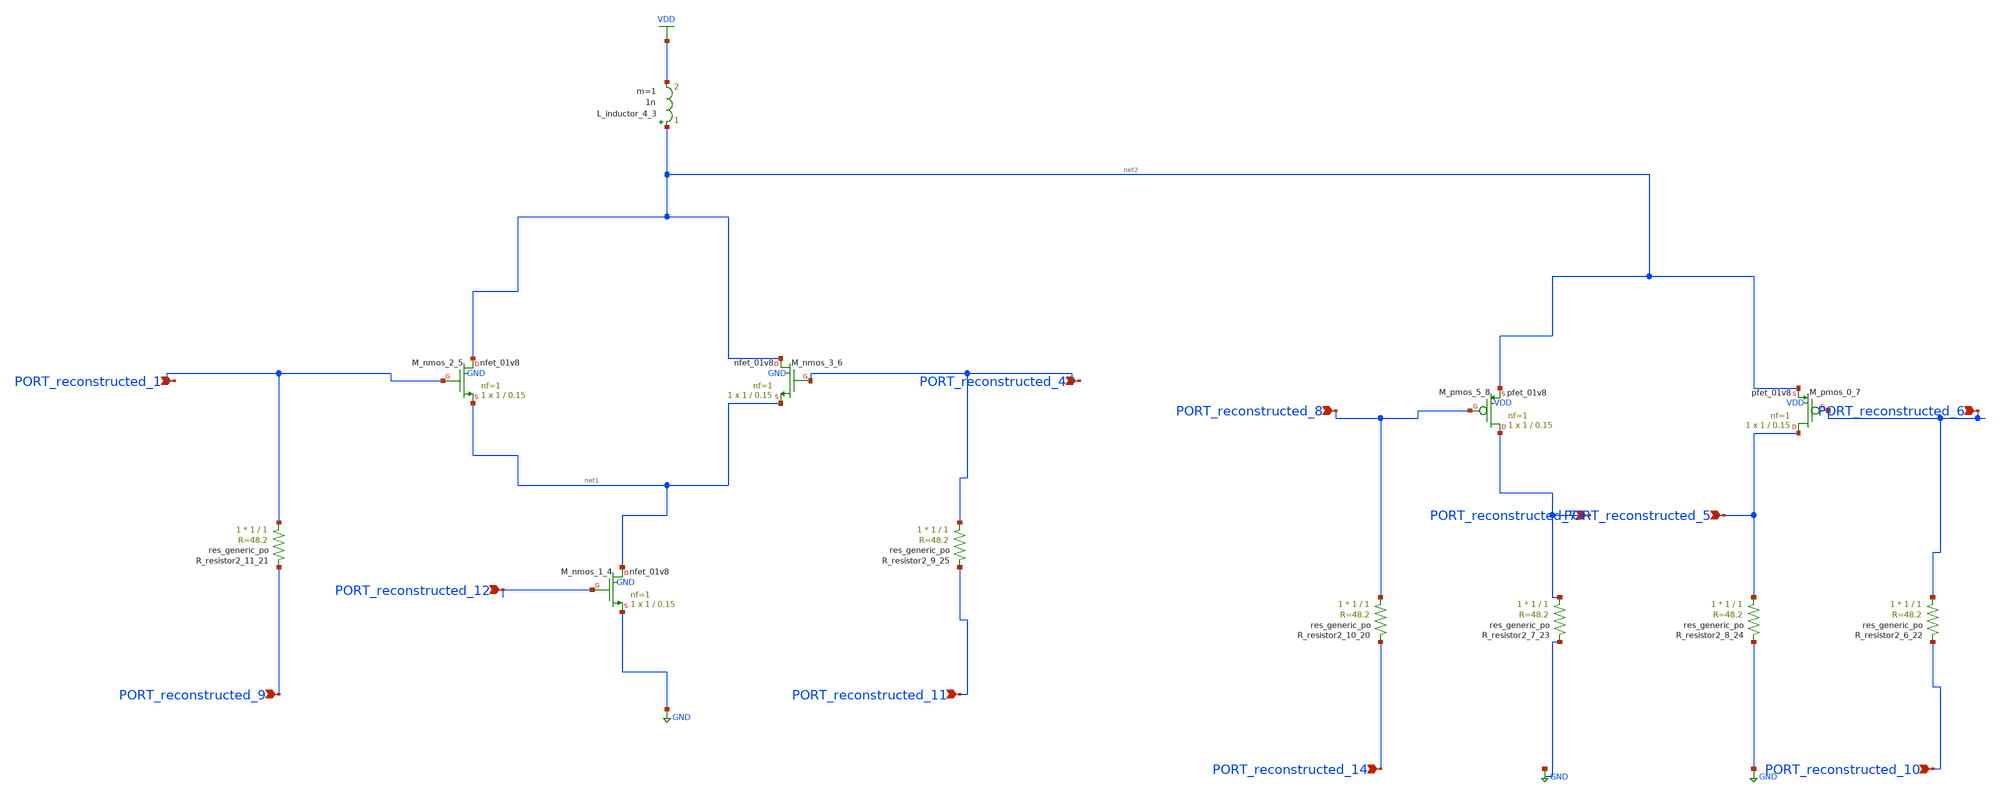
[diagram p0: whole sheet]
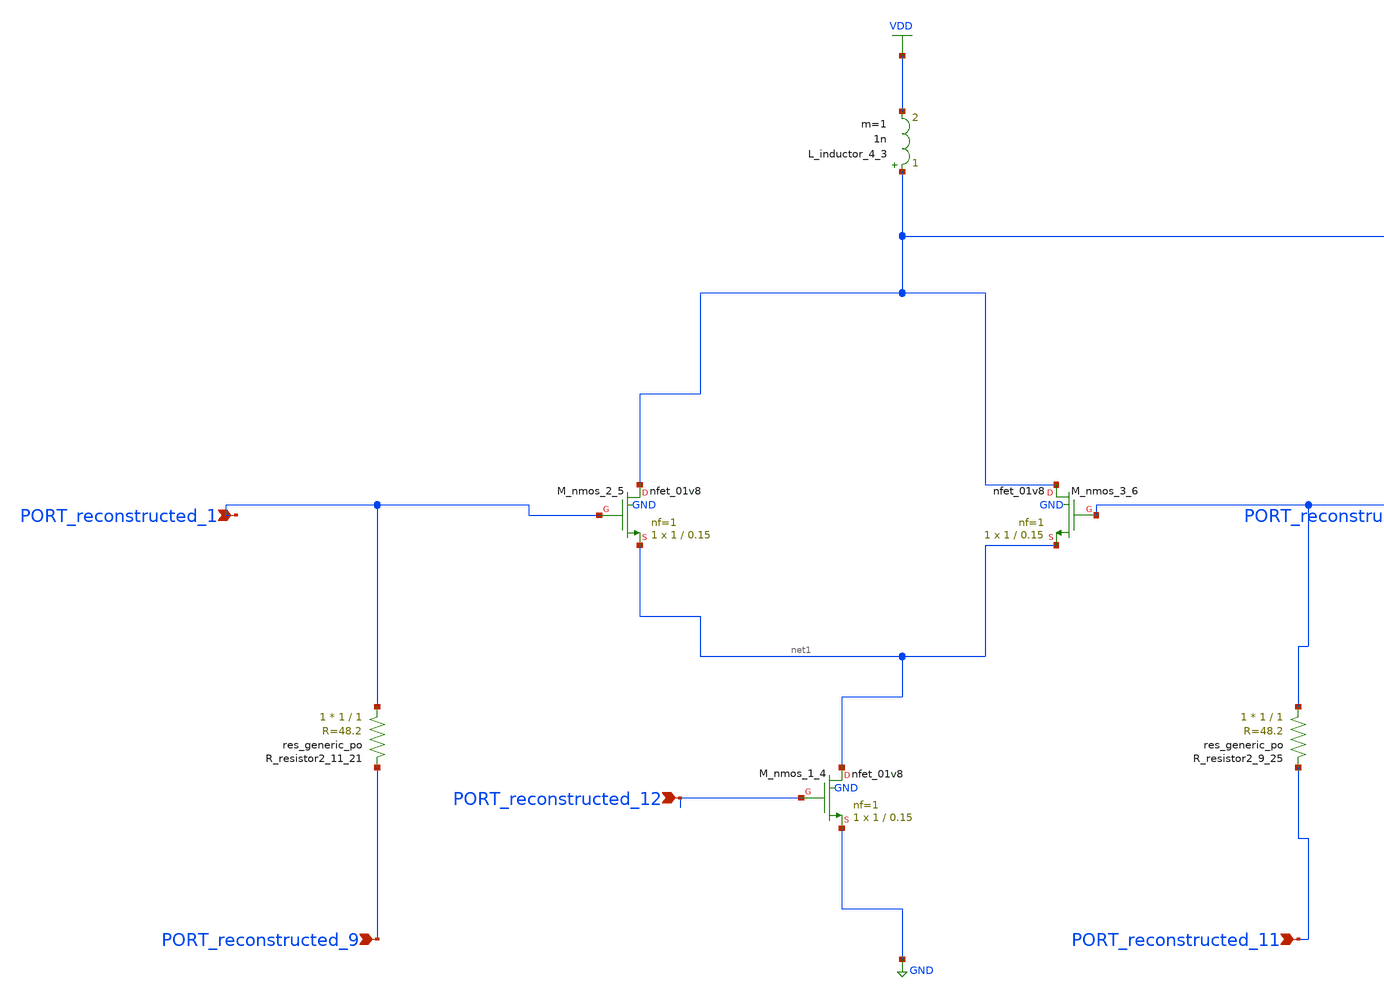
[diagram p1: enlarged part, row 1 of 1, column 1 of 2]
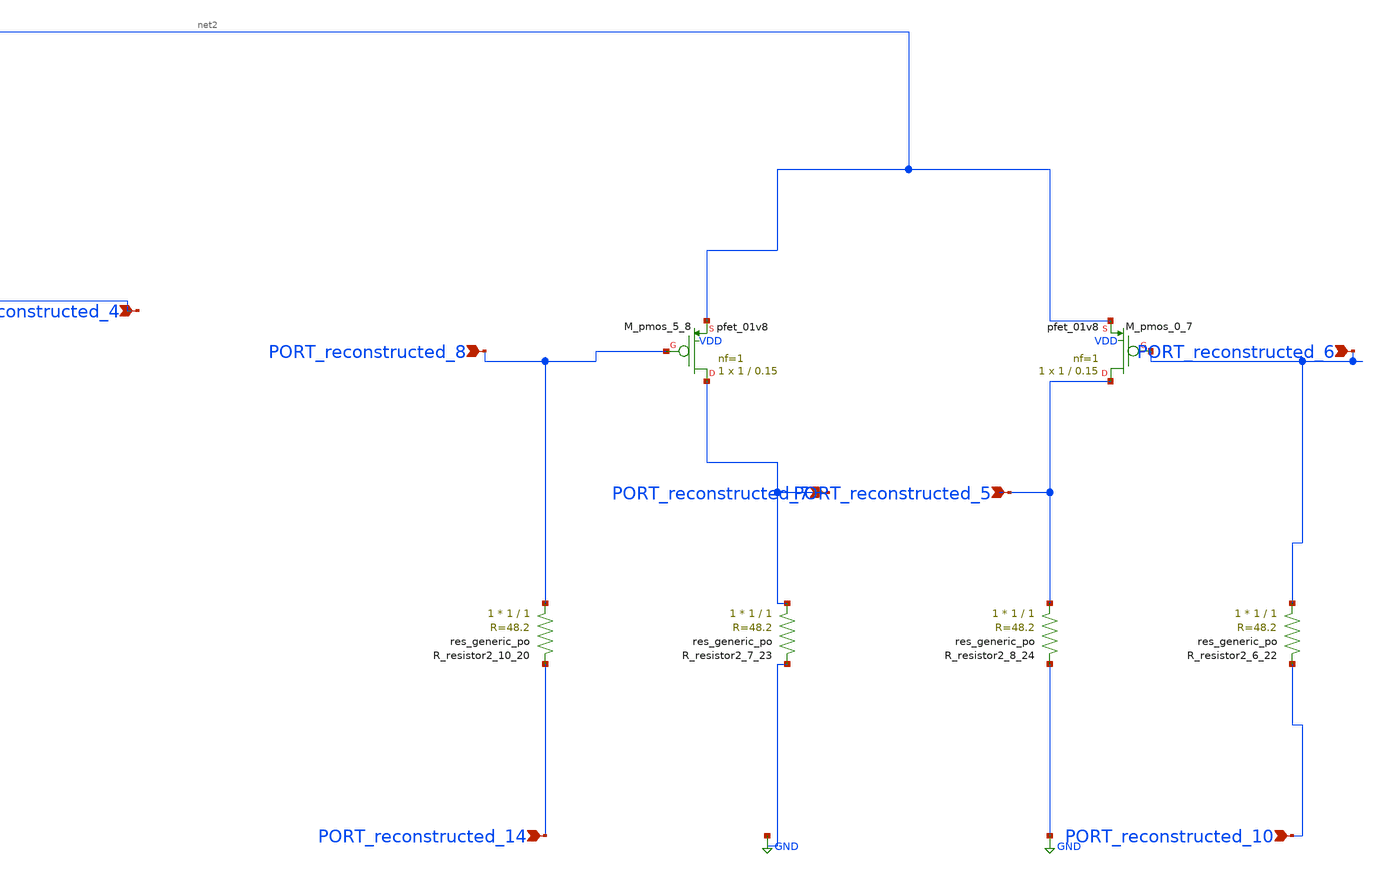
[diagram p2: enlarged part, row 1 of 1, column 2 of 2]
** sch_path: schematics/10_1016_j_aeue_2023_154684_09_004.sch
**.subckt 10_1016_j_aeue_2023_154684_09_004 PORT_reconstructed_1 PORT_reconstructed_6
*+ PORT_reconstructed_9 PORT_reconstructed_5 PORT_reconstructed_4 PORT_reconstructed_10 PORT_reconstructed_8
*+ PORT_reconstructed_7 PORT_reconstructed_11 PORT_reconstructed_12 PORT_reconstructed_14
*.ipin PORT_reconstructed_1
*.ipin PORT_reconstructed_6
*.ipin PORT_reconstructed_9
*.ipin PORT_reconstructed_5
*.ipin PORT_reconstructed_4
*.ipin PORT_reconstructed_10
*.ipin PORT_reconstructed_8
*.ipin PORT_reconstructed_7
*.ipin PORT_reconstructed_11
*.ipin PORT_reconstructed_12
*.ipin PORT_reconstructed_14
L_inductor_4_3 net2 VDD 1n m=1
XM_nmos_1_4 net1 PORT_reconstructed_12 GND GND sky130_fd_pr__nfet_01v8 L=0.15 W=1 nf=1 ad='int((1 + 1)/2) * 1 / 1 * 0.29'
+ as='int((1 + 2)/2) * 1 / 1 * 0.29' pd='2*int((1 + 1)/2) * (1 / 1 + 0.29)' ps='2*int((1 + 2)/2) * (1 / 1 + 0.29)'
+ nrd='0.29 / 1 ' nrs='0.29 / 1 ' sa=0 sb=0 sd=0 mult=1 m=1
XM_nmos_2_5 net2 PORT_reconstructed_1 net1 GND sky130_fd_pr__nfet_01v8 L=0.15 W=1 nf=1 ad='int((1 + 1)/2) * 1 / 1 * 0.29'
+ as='int((1 + 2)/2) * 1 / 1 * 0.29' pd='2*int((1 + 1)/2) * (1 / 1 + 0.29)' ps='2*int((1 + 2)/2) * (1 / 1 + 0.29)'
+ nrd='0.29 / 1 ' nrs='0.29 / 1 ' sa=0 sb=0 sd=0 mult=1 m=1
XM_nmos_3_6 net2 PORT_reconstructed_4 net1 GND sky130_fd_pr__nfet_01v8 L=0.15 W=1 nf=1 ad='int((1 + 1)/2) * 1 / 1 * 0.29'
+ as='int((1 + 2)/2) * 1 / 1 * 0.29' pd='2*int((1 + 1)/2) * (1 / 1 + 0.29)' ps='2*int((1 + 2)/2) * (1 / 1 + 0.29)'
+ nrd='0.29 / 1 ' nrs='0.29 / 1 ' sa=0 sb=0 sd=0 mult=1 m=1
XM_pmos_0_7 PORT_reconstructed_5 PORT_reconstructed_6 net2 VDD sky130_fd_pr__pfet_01v8 L=0.15 W=1 nf=1
+ ad='int((1 + 1)/2) * 1 / 1 * 0.29' as='int((1 + 2)/2) * 1 / 1 * 0.29' pd='2*int((1 + 1)/2) * (1 / 1 + 0.29)'
+ ps='2*int((1 + 2)/2) * (1 / 1 + 0.29)' nrd='0.29 / 1 ' nrs='0.29 / 1 ' sa=0 sb=0 sd=0 mult=1 m=1
XM_pmos_5_8 PORT_reconstructed_7 PORT_reconstructed_8 net2 VDD sky130_fd_pr__pfet_01v8 L=0.15 W=1 nf=1
+ ad='int((1 + 1)/2) * 1 / 1 * 0.29' as='int((1 + 2)/2) * 1 / 1 * 0.29' pd='2*int((1 + 1)/2) * (1 / 1 + 0.29)'
+ ps='2*int((1 + 2)/2) * (1 / 1 + 0.29)' nrd='0.29 / 1 ' nrs='0.29 / 1 ' sa=0 sb=0 sd=0 mult=1 m=1
XR_resistor2_10_20 PORT_reconstructed_8 PORT_reconstructed_14 sky130_fd_pr__res_generic_po W=1 L=1
+ m=1
XR_resistor2_11_21 PORT_reconstructed_1 PORT_reconstructed_9 sky130_fd_pr__res_generic_po W=1 L=1
+ m=1
XR_resistor2_6_22 PORT_reconstructed_6 PORT_reconstructed_10 sky130_fd_pr__res_generic_po W=1 L=1
+ m=1
XR_resistor2_7_23 PORT_reconstructed_7 GND sky130_fd_pr__res_generic_po W=1 L=1 m=1
XR_resistor2_8_24 PORT_reconstructed_5 GND sky130_fd_pr__res_generic_po W=1 L=1 m=1
XR_resistor2_9_25 PORT_reconstructed_4 PORT_reconstructed_11 sky130_fd_pr__res_generic_po W=1 L=1
+ m=1
**.ends
.GLOBAL GND
.GLOBAL VDD
.end
